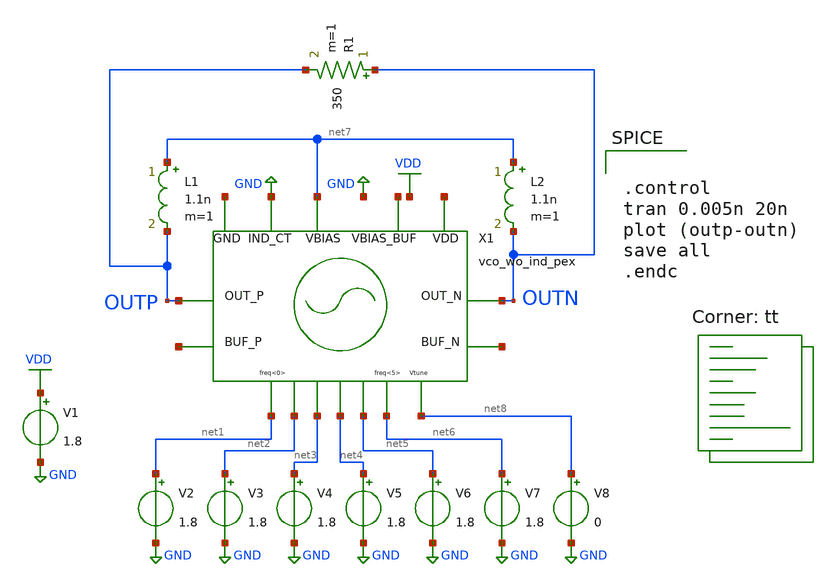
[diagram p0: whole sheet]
** sch_path: xschem/vco_wo_ind_pex_tb.sch
**.subckt vco_wo_ind_pex_tb
V1 VDD GND 1.8
V2 net1 GND 1.8
V3 net2 GND 1.8
V4 net3 GND 1.8
V5 net4 GND 1.8
V6 net5 GND 1.8
V7 net6 GND 1.8
L1 net7 OUTP 1.1n m=1
L2 net7 OUTN 1.1n m=1
V8 net8 GND 0
X1 OUTP net9 GND net10 OUTN net1 net2 net3 net4 net5 net6 net7 net8 net11 net12 net13 vco_wo_ind_pex
R1 OUTN OUTP 350 m=1
**** begin user architecture code


.control
tran 0.005n 20n
plot (outp-outn)
save all
.endc


.lib $::SKYWATER_MODELS/sky130.lib.spice tt
**** end user architecture code
**.ends
.GLOBAL GND
.GLOBAL VDD
.end
